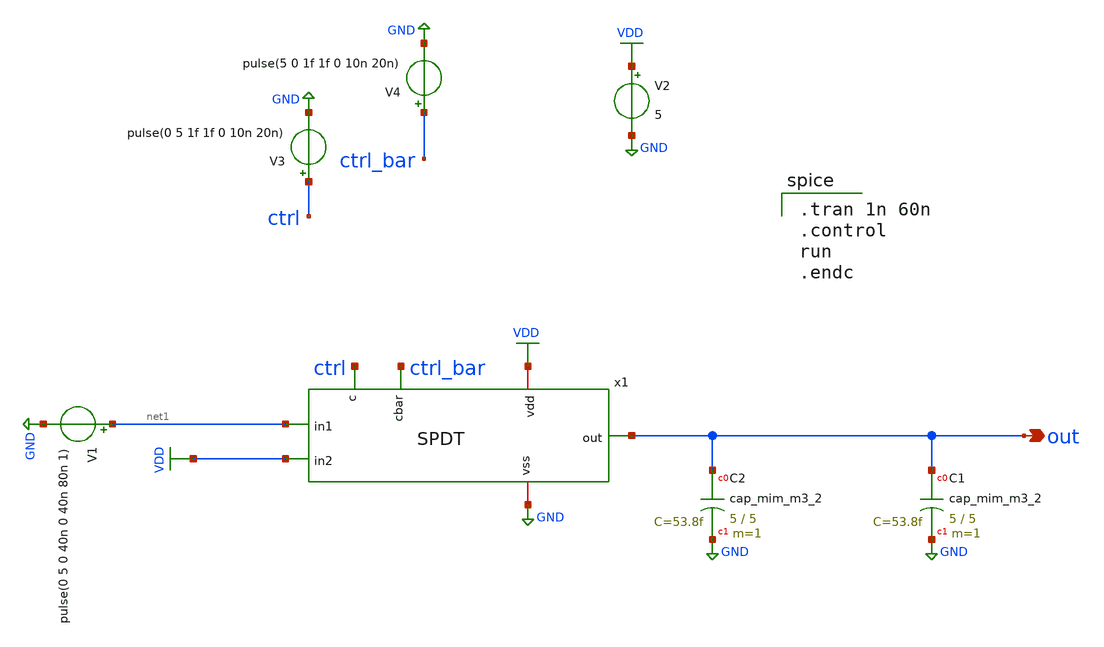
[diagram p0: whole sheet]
** sch_path: ADC/16bit_C2C/MagicAndSpice/SPDT_TB.sch
**.subckt SPDT_TB out
*.opin out
V1 net1 GND pulse(0 5 0 40n 0 40n 80n 1)
V2 VDD GND 5
V3 ctrl GND pulse(0 5 1f 1f 0 10n 20n)
V4 ctrl_bar GND pulse(5 0 1f 1f 0 10n 20n)
x1 ctrl_bar VDD GND ctrl net1 out VDD SPDT
XC1 out GND sky130_fd_pr__cap_mim_m3_2 W=5 L=5 MF=1 m=1
XC2 out GND sky130_fd_pr__cap_mim_m3_2 W=5 L=5 MF=1 m=1
**** begin user architecture code

** opencircuitdesign pdks install
.lib $::SKYWATER_MODELS/sky130.lib.spice tt



.tran 1n 60n
.control
run
.endc

**** end user architecture code
**.ends

* expanding   symbol:  /home/ee431/workspace/6SAR_CDAC/SPDT.sym # of pins=7
** sym_path: ADC/4bit_C2C/MagicAndSpice/SPDT.sym
** sch_path: ADC/4bit_C2C/MagicAndSpice/SPDT.sch
.subckt SPDT cbar vdd vss c in1 out in2
*.ipin in1
*.ipin in2
*.ipin c
*.ipin cbar
*.opin out
*.iopin vdd
*.iopin vss
x1 c out in1 vdd cbar vss T_gate
x2 cbar out in2 vdd c vss T_gate
.ends


* expanding   symbol:  /home/ee431/workspace/6SAR_CDAC/T_gate.sym # of pins=6
** sym_path: ADC/16bit_C2C/MagicAndSpice/T_gate.sym
** sch_path: ADC/16bit_C2C/MagicAndSpice/T_gate.sch
.subckt T_gate c out in Vdd cbar Vss
*.ipin in
*.ipin cbar
*.ipin c
*.iopin Vdd
*.iopin Vss
*.iopin out
XM1 in c out GND sky130_fd_pr__nfet_g5v0d10v5 L=0.5 W=10 nf=1 ad='int((nf+1)/2) * W/nf * 0.29' as='int((nf+2)/2) * W/nf * 0.29'
+ pd='2*int((nf+1)/2) * (W/nf + 0.29)' ps='2*int((nf+2)/2) * (W/nf + 0.29)' nrd='0.29 / W' nrs='0.29 / W'
+ sa=0 sb=0 sd=0 mult=1 m=1
XM2 out cbar in Vdd sky130_fd_pr__pfet_g5v0d10v5 L=0.5 W=10 nf=1 ad='int((nf+1)/2) * W/nf * 0.29' as='int((nf+2)/2) * W/nf * 0.29'
+ pd='2*int((nf+1)/2) * (W/nf + 0.29)' ps='2*int((nf+2)/2) * (W/nf + 0.29)' nrd='0.29 / W' nrs='0.29 / W'
+ sa=0 sb=0 sd=0 mult=1 m=1
.ends

.GLOBAL GND
.GLOBAL VDD
.end
